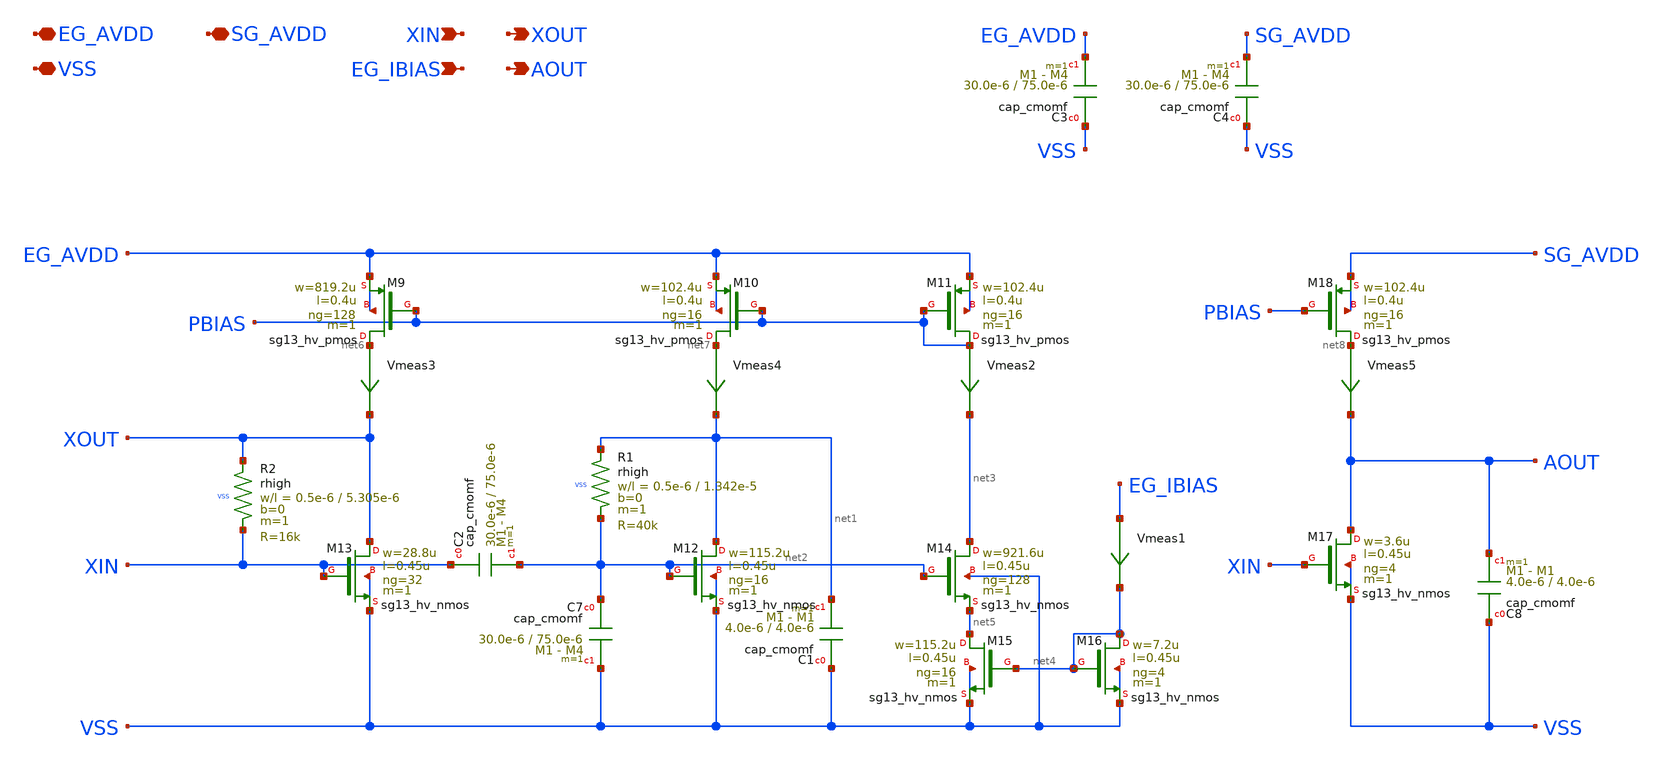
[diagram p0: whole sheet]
** sch_path: macros/vittoz_pierce_osc/schematic/xschem/vittoz_pierce_osc.sch
**.subckt vittoz_pierce_osc EG_AVDD VSS SG_AVDD XIN EG_IBIAS XOUT AOUT
*.iopin EG_AVDD
*.iopin VSS
*.iopin SG_AVDD
*.ipin XIN
*.ipin EG_IBIAS
*.opin XOUT
*.opin AOUT
Vmeas3 net6 XOUT 0
.save i(vmeas3)
Vmeas4 net7 net1 0
.save i(vmeas4)
Vmeas2 PBIAS net3 0
.save i(vmeas2)
Vmeas5 net8 AOUT 0
.save i(vmeas5)
Vmeas1 EG_IBIAS net4 0
.save i(vmeas1)
XC3 VSS EG_AVDD cap_cmomf w=30.0e-6 l=75.0e-6 mmin=1 mmax=4 subblock=0 rfmodel=0 subscale=1 m=1
+ mm_ok=1
XC4 VSS SG_AVDD cap_cmomf w=30.0e-6 l=75.0e-6 mmin=1 mmax=4 subblock=0 rfmodel=0 subscale=1 m=1
+ mm_ok=1
XR1 net1 net2 VSS rhigh w=0.5e-6 l=1.342e-5 m=1 b=0 mm_ok=1
XR2 XOUT XIN VSS rhigh w=0.5e-6 l=5.305e-6 m=1 b=0 mm_ok=1
XC2 XIN net2 cap_cmomf w=30.0e-6 l=75.0e-6 mmin=1 mmax=4 subblock=0 rfmodel=0 subscale=1 m=1 mm_ok=1
XC7 net2 VSS cap_cmomf w=30.0e-6 l=75.0e-6 mmin=1 mmax=4 subblock=0 rfmodel=0 subscale=1 m=1 mm_ok=1
XC1 VSS net1 cap_cmomf w=4.0e-6 l=4.0e-6 mmin=1 mmax=1 subblock=0 rfmodel=0 subscale=1 m=1 mm_ok=1
XC8 VSS AOUT cap_cmomf w=4.0e-6 l=4.0e-6 mmin=1 mmax=1 subblock=0 rfmodel=0 subscale=1 m=1 mm_ok=1
XM11 PBIAS PBIAS EG_AVDD EG_AVDD sg13_hv_pmos w=102.4u l=0.4u ng=16 m=1 mm_ok=1
XM10 net7 PBIAS EG_AVDD EG_AVDD sg13_hv_pmos w=102.4u l=0.4u ng=16 m=1 mm_ok=1
XM9 net6 PBIAS EG_AVDD EG_AVDD sg13_hv_pmos w=819.2u l=0.4u ng=128 m=1 mm_ok=1
XM14 net3 net2 net5 VSS sg13_hv_nmos w=921.6u l=0.45u ng=128 m=1 mm_ok=1
XM12 net1 net2 VSS VSS sg13_hv_nmos w=115.2u l=0.45u ng=16 m=1 mm_ok=1
XM13 XOUT XIN VSS VSS sg13_hv_nmos w=28.8u l=0.45u ng=32 m=1 mm_ok=1
XM15 net5 net4 VSS VSS sg13_hv_nmos w=115.2u l=0.45u ng=16 m=1 mm_ok=1
XM16 net4 net4 VSS VSS sg13_hv_nmos w=7.2u l=0.45u ng=4 m=1 mm_ok=1
XM18 net8 PBIAS SG_AVDD SG_AVDD sg13_hv_pmos w=102.4u l=0.4u ng=16 m=1 mm_ok=1
XM17 AOUT XIN VSS VSS sg13_hv_nmos w=3.6u l=0.45u ng=4 m=1 mm_ok=1
**.ends
.end
